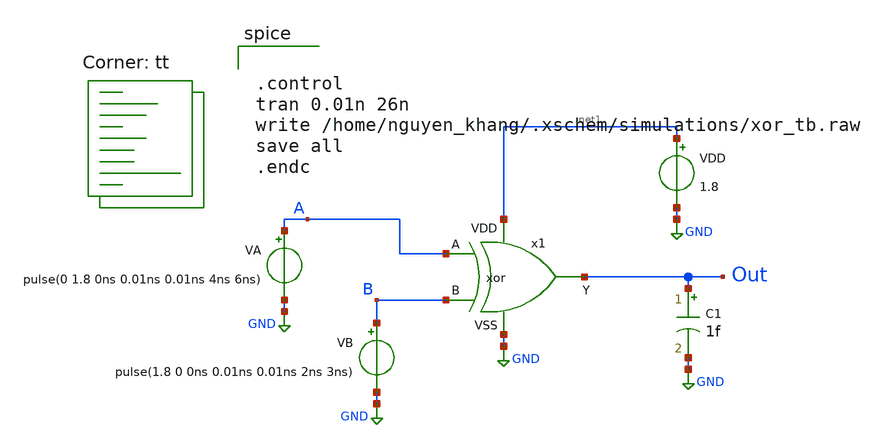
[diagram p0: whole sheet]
** sch_path: xor_tb.sch
**.subckt xor_tb
x1 net1 GND Out A B xor
VA A GND pulse(0 1.8 0ns 0.01ns 0.01ns 4ns 6ns)
VB B GND pulse(1.8 0 0ns 0.01ns 0.01ns 2ns 3ns)
VDD net1 GND 1.8
C1 Out GND 1f m=1
**** begin user architecture code
.lib $::SKYWATER_MODELS/sky130.lib.spice tt


.control
tran 0.01n 26n
write /home/nguyen_khang/.xschem/simulations/xor_tb.raw
save all
.endc

**** end user architecture code
**.ends

* expanding   symbol:  project/xor.sym # of pins=5
** sym_path: xor.sym
** sch_path: xor.sch
.subckt xor VDD VSS Y A B
*.ipin A
*.ipin VDD
*.opin Y
*.ipin B
*.ipin VSS
XM1 net1 A VDD VDD sky130_fd_pr__pfet_01v8 L=0.15 W=2 nf=1 ad='int((nf+1)/2) * W/nf * 0.29' as='int((nf+2)/2) * W/nf * 0.29'
+ pd='2*int((nf+1)/2) * (W/nf + 0.29)' ps='2*int((nf+2)/2) * (W/nf + 0.29)' nrd='0.29 / W' nrs='0.29 / W'
+ sa=0 sb=0 sd=0 mult=1 m=1
XM2 Y A_bar net1 VDD sky130_fd_pr__pfet_01v8 L=0.15 W=2 nf=1 ad='int((nf+1)/2) * W/nf * 0.29' as='int((nf+2)/2) * W/nf * 0.29'
+ pd='2*int((nf+1)/2) * (W/nf + 0.29)' ps='2*int((nf+2)/2) * (W/nf + 0.29)' nrd='0.29 / W' nrs='0.29 / W'
+ sa=0 sb=0 sd=0 mult=1 m=1
XM3 net1 B VDD VDD sky130_fd_pr__pfet_01v8 L=0.15 W=2 nf=1 ad='int((nf+1)/2) * W/nf * 0.29' as='int((nf+2)/2) * W/nf * 0.29'
+ pd='2*int((nf+1)/2) * (W/nf + 0.29)' ps='2*int((nf+2)/2) * (W/nf + 0.29)' nrd='0.29 / W' nrs='0.29 / W'
+ sa=0 sb=0 sd=0 mult=1 m=1
XM4 Y B_bar net1 VDD sky130_fd_pr__pfet_01v8 L=0.15 W=2 nf=1 ad='int((nf+1)/2) * W/nf * 0.29' as='int((nf+2)/2) * W/nf * 0.29'
+ pd='2*int((nf+1)/2) * (W/nf + 0.29)' ps='2*int((nf+2)/2) * (W/nf + 0.29)' nrd='0.29 / W' nrs='0.29 / W'
+ sa=0 sb=0 sd=0 mult=1 m=1
XM5 Y A net2 VSS sky130_fd_pr__nfet_01v8 L=0.15 W=1 nf=1 ad='int((nf+1)/2) * W/nf * 0.29' as='int((nf+2)/2) * W/nf * 0.29'
+ pd='2*int((nf+1)/2) * (W/nf + 0.29)' ps='2*int((nf+2)/2) * (W/nf + 0.29)' nrd='0.29 / W' nrs='0.29 / W'
+ sa=0 sb=0 sd=0 mult=1 m=1
XM6 net2 B VSS VSS sky130_fd_pr__nfet_01v8 L=0.15 W=1 nf=1 ad='int((nf+1)/2) * W/nf * 0.29' as='int((nf+2)/2) * W/nf * 0.29'
+ pd='2*int((nf+1)/2) * (W/nf + 0.29)' ps='2*int((nf+2)/2) * (W/nf + 0.29)' nrd='0.29 / W' nrs='0.29 / W'
+ sa=0 sb=0 sd=0 mult=1 m=1
XM7 Y A_bar net3 VSS sky130_fd_pr__nfet_01v8 L=0.15 W=1 nf=1 ad='int((nf+1)/2) * W/nf * 0.29' as='int((nf+2)/2) * W/nf * 0.29'
+ pd='2*int((nf+1)/2) * (W/nf + 0.29)' ps='2*int((nf+2)/2) * (W/nf + 0.29)' nrd='0.29 / W' nrs='0.29 / W'
+ sa=0 sb=0 sd=0 mult=1 m=1
XM8 net3 B_bar VSS VSS sky130_fd_pr__nfet_01v8 L=0.15 W=1 nf=1 ad='int((nf+1)/2) * W/nf * 0.29' as='int((nf+2)/2) * W/nf * 0.29'
+ pd='2*int((nf+1)/2) * (W/nf + 0.29)' ps='2*int((nf+2)/2) * (W/nf + 0.29)' nrd='0.29 / W' nrs='0.29 / W'
+ sa=0 sb=0 sd=0 mult=1 m=1
XM9 A_bar A VSS VSS sky130_fd_pr__nfet_01v8 L=0.15 W=1 nf=1 ad='int((nf+1)/2) * W/nf * 0.29' as='int((nf+2)/2) * W/nf * 0.29'
+ pd='2*int((nf+1)/2) * (W/nf + 0.29)' ps='2*int((nf+2)/2) * (W/nf + 0.29)' nrd='0.29 / W' nrs='0.29 / W'
+ sa=0 sb=0 sd=0 mult=1 m=1
XM10 A_bar A VDD VDD sky130_fd_pr__pfet_01v8 L=0.15 W=2 nf=1 ad='int((nf+1)/2) * W/nf * 0.29' as='int((nf+2)/2) * W/nf * 0.29'
+ pd='2*int((nf+1)/2) * (W/nf + 0.29)' ps='2*int((nf+2)/2) * (W/nf + 0.29)' nrd='0.29 / W' nrs='0.29 / W'
+ sa=0 sb=0 sd=0 mult=1 m=1
XM11 B_bar B VSS VSS sky130_fd_pr__nfet_01v8 L=0.15 W=1 nf=1 ad='int((nf+1)/2) * W/nf * 0.29' as='int((nf+2)/2) * W/nf * 0.29'
+ pd='2*int((nf+1)/2) * (W/nf + 0.29)' ps='2*int((nf+2)/2) * (W/nf + 0.29)' nrd='0.29 / W' nrs='0.29 / W'
+ sa=0 sb=0 sd=0 mult=1 m=1
XM12 B_bar B VDD VDD sky130_fd_pr__pfet_01v8 L=0.15 W=2 nf=1 ad='int((nf+1)/2) * W/nf * 0.29' as='int((nf+2)/2) * W/nf * 0.29'
+ pd='2*int((nf+1)/2) * (W/nf + 0.29)' ps='2*int((nf+2)/2) * (W/nf + 0.29)' nrd='0.29 / W' nrs='0.29 / W'
+ sa=0 sb=0 sd=0 mult=1 m=1
.ends

.GLOBAL GND
.end
